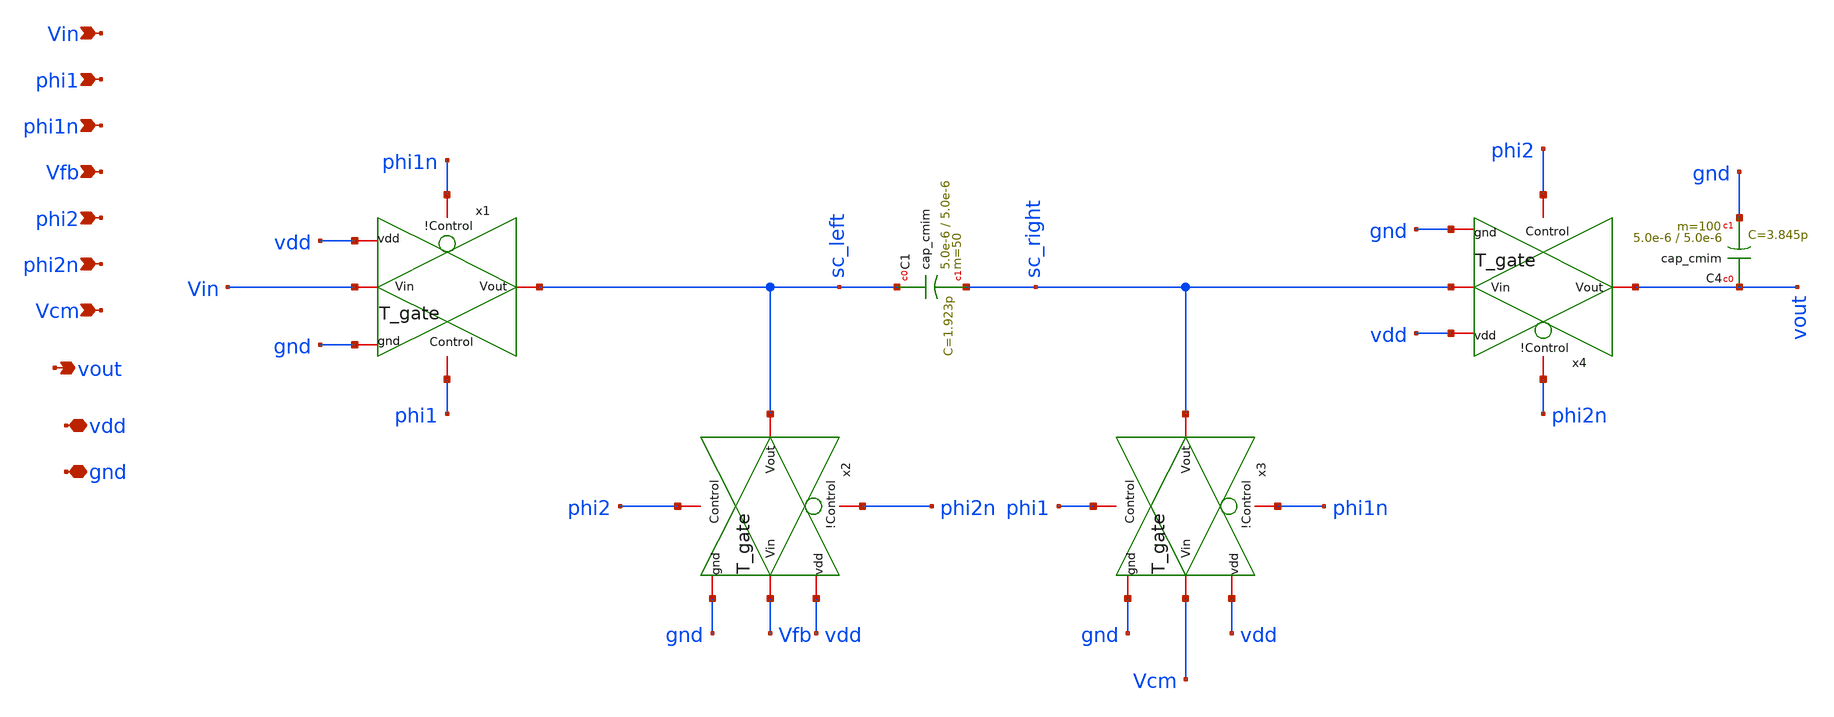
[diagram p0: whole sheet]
** sch_path: xschem/switched_capacitor.sch
**.subckt switched_capacitor Vin phi1 phi1n Vfb phi2 phi2n Vcm vout vdd gnd
*.ipin Vin
*.ipin phi1
*.ipin phi1n
*.ipin Vfb
*.ipin phi2
*.ipin phi2n
*.ipin Vcm
*.opin vout
*.iopin vdd
*.iopin gnd
x1 phi1n Vin sc_left gnd phi1 vdd T_gate
x2 phi2n Vfb sc_left gnd phi2 vdd T_gate
x3 phi1n Vcm sc_right gnd phi1 vdd T_gate
XC1 sc_left sc_right cap_cmim w=5.0e-6 l=5.0e-6 m=50 mm_ok=1
x4 phi2n sc_right vout gnd phi2 vdd T_gate
XC4 vout gnd cap_cmim w=5.0e-6 l=5.0e-6 m=100 mm_ok=1
**.ends

* expanding   symbol:  T_gate.sym # of pins=6
** sym_path: T_gate.sym
** sch_path: T_gate.sch
.subckt T_gate !Control Vin Vout gnd Control vdd
*.iopin Vout
*.iopin Vin
*.iopin !Control
*.iopin Control
*.iopin gnd
*.iopin vdd
XM1 Vin Control Vout gnd sg13_lv_nmos w=1u l=0.13u ng=1 m=1 mm_ok=1
XM2 Vout !Control Vin vdd sg13_lv_pmos w=3u l=0.13u ng=1 m=1 mm_ok=1
.ends

.end
